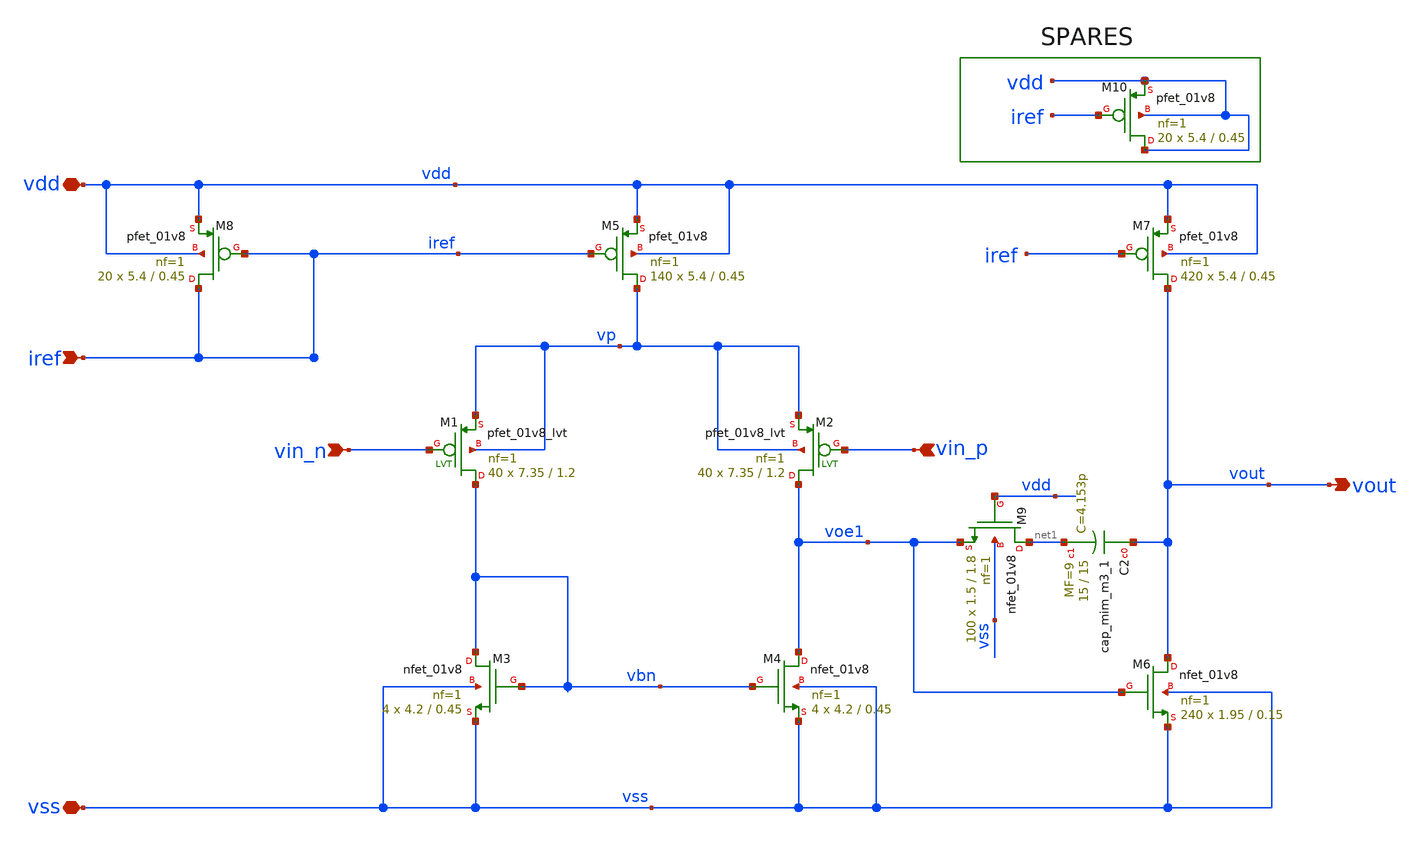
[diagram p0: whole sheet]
** sch_path: xschem/opamp_ramiro.sch
**.subckt opamp_ramiro vdd vss vin_n vin_p iref vout
*.iopin vdd
*.iopin vss
*.ipin vin_n
*.ipin vin_p
*.ipin iref
*.opin vout
XM3 vbn vbn vss vss sky130_fd_pr__nfet_01v8 L=0.45 W=4.2 nf=1 ad='W * 0.29' as='W * 0.29' pd='2 * (W + 0.29)'
+ ps='2 * (W + 0.29)' nrd='0.29 / W' nrs='0.29 / W' sa=0 sb=0 sd=0 mult=4 m=4
XM4 voe1 vbn vss vss sky130_fd_pr__nfet_01v8 L=0.45 W=4.2 nf=1 ad='W * 0.29' as='W * 0.29' pd='2 * (W + 0.29)'
+ ps='2 * (W + 0.29)' nrd='0.29 / W' nrs='0.29 / W' sa=0 sb=0 sd=0 mult=4 m=4
XM5 vp iref vdd vdd sky130_fd_pr__pfet_01v8 L=0.45 W=5.4 nf=1 ad='W * 0.29' as='W * 0.29' pd='2 * (W + 0.29)'
+ ps='2 * (W + 0.29)' nrd='0.29 / W' nrs='0.29 / W' sa=0 sb=0 sd=0 mult=140 m=140
XM7 vout iref vdd vdd sky130_fd_pr__pfet_01v8 L=0.45 W=5.4 nf=1 ad='W * 0.29' as='W * 0.29' pd='2 * (W + 0.29)'
+ ps='2 * (W + 0.29)' nrd='0.29 / W' nrs='0.29 / W' sa=0 sb=0 sd=0 mult=420 m=420
XM8 iref iref vdd vdd sky130_fd_pr__pfet_01v8 L=0.45 W=5.4 nf=1 ad='W * 0.29' as='W * 0.29' pd='2 * (W + 0.29)'
+ ps='2 * (W + 0.29)' nrd='0.29 / W' nrs='0.29 / W' sa=0 sb=0 sd=0 mult=20 m=20
XM6 vout voe1 vss vss sky130_fd_pr__nfet_01v8 L=0.15 W=1.95 nf=1 ad='W * 0.29' as='W * 0.29' pd='2 * (W + 0.29)'
+ ps='2 * (W + 0.29)' nrd='0.29 / W' nrs='0.29 / W' sa=0 sb=0 sd=0 mult=240 m=240
XM1 vbn vin_n vp vp sky130_fd_pr__pfet_01v8_lvt L=1.2 W=7.35 nf=1 ad='int((nf+1)/2) * W/nf * 0.29' as='int((nf+2)/2) * W/nf * 0.29'
+ pd='2*int((nf+1)/2) * (W/nf + 0.29)' ps='2*int((nf+2)/2) * (W/nf + 0.29)' nrd='0.29 / W' nrs='0.29 / W'
+ sa=0 sb=0 sd=0 mult=40 m=40
XM2 voe1 vin_p vp vp sky130_fd_pr__pfet_01v8_lvt L=1.2 W=7.35 nf=1 ad='int((nf+1)/2) * W/nf * 0.29' as='int((nf+2)/2) * W/nf * 0.29'
+ pd='2*int((nf+1)/2) * (W/nf + 0.29)' ps='2*int((nf+2)/2) * (W/nf + 0.29)' nrd='0.29 / W' nrs='0.29 / W'
+ sa=0 sb=0 sd=0 mult=40 m=40
XM9 net1 vdd voe1 vss sky130_fd_pr__nfet_01v8 L=1.8 W=1.5 nf=1 ad='W * 0.29' as='W * 0.29' pd='2 * (W + 0.29)'
+ ps='2 * (W + 0.29)' nrd='0.29 / W' nrs='0.29 / W' sa=0 sb=0 sd=0 mult=100 m=100
XM10 vdd iref vdd vdd sky130_fd_pr__pfet_01v8 L=0.45 W=5.4 nf=1 ad='W * 0.29' as='W * 0.29' pd='2 * (W + 0.29)'
+ ps='2 * (W + 0.29)' nrd='0.29 / W' nrs='0.29 / W' sa=0 sb=0 sd=0 mult=20 m=20
XC2 vout net1 sky130_fd_pr__cap_mim_m3_1 W=15 L=15 MF=9 m=9
**.ends
.end
